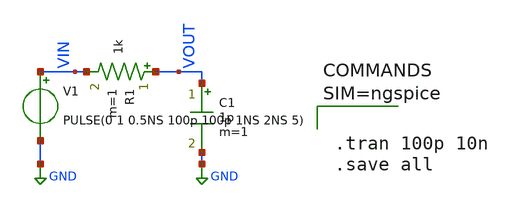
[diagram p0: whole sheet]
** sch_path: xschem/rclpf.sch
**.subckt rclpf
R1 VOUT VIN 1k m=1
C1 VOUT GND 1p m=1
V1 VIN GND PULSE(0 1 0.5NS 100p 100p 1NS 2NS 5)
**** begin user architecture code



.tran 100p 10n
.save all




**** end user architecture code
**.ends
.GLOBAL GND
.end
